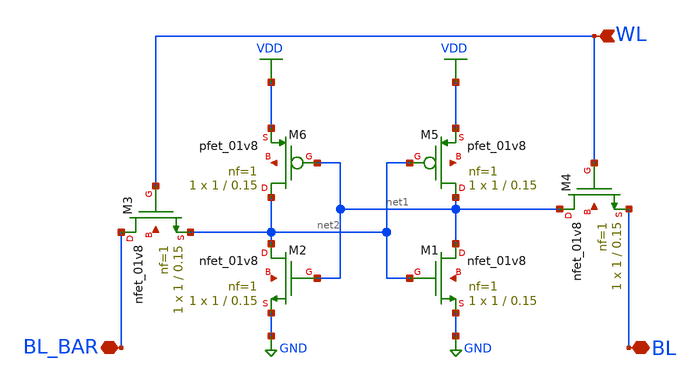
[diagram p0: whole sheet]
** sch_path: analog/schematics/SRAM_access.sch
**.subckt SRAM_access BL_BAR BL WL
*.iopin BL_BAR
*.iopin BL
*.ipin WL
XM1 net1 net2 GND net3 sky130_fd_pr__nfet_01v8 L=0.15 W=1 nf=1 ad='int((nf+1)/2) * W/nf * 0.29' as='int((nf+2)/2) * W/nf * 0.29'
+ pd='2*int((nf+1)/2) * (W/nf + 0.29)' ps='2*int((nf+2)/2) * (W/nf + 0.29)' nrd='0.29 / W' nrs='0.29 / W'
+ sa=0 sb=0 sd=0 mult=1 m=1
XM2 net2 net1 GND net4 sky130_fd_pr__nfet_01v8 L=0.15 W=1 nf=1 ad='int((nf+1)/2) * W/nf * 0.29' as='int((nf+2)/2) * W/nf * 0.29'
+ pd='2*int((nf+1)/2) * (W/nf + 0.29)' ps='2*int((nf+2)/2) * (W/nf + 0.29)' nrd='0.29 / W' nrs='0.29 / W'
+ sa=0 sb=0 sd=0 mult=1 m=1
XM3 BL_BAR WL net2 net5 sky130_fd_pr__nfet_01v8 L=0.15 W=1 nf=1 ad='int((nf+1)/2) * W/nf * 0.29' as='int((nf+2)/2) * W/nf * 0.29'
+ pd='2*int((nf+1)/2) * (W/nf + 0.29)' ps='2*int((nf+2)/2) * (W/nf + 0.29)' nrd='0.29 / W' nrs='0.29 / W'
+ sa=0 sb=0 sd=0 mult=1 m=1
XM4 net1 WL BL net6 sky130_fd_pr__nfet_01v8 L=0.15 W=1 nf=1 ad='int((nf+1)/2) * W/nf * 0.29' as='int((nf+2)/2) * W/nf * 0.29'
+ pd='2*int((nf+1)/2) * (W/nf + 0.29)' ps='2*int((nf+2)/2) * (W/nf + 0.29)' nrd='0.29 / W' nrs='0.29 / W'
+ sa=0 sb=0 sd=0 mult=1 m=1
XM5 net1 net2 VDD net7 sky130_fd_pr__pfet_01v8 L=0.15 W=1 nf=1 ad='int((nf+1)/2) * W/nf * 0.29' as='int((nf+2)/2) * W/nf * 0.29'
+ pd='2*int((nf+1)/2) * (W/nf + 0.29)' ps='2*int((nf+2)/2) * (W/nf + 0.29)' nrd='0.29 / W' nrs='0.29 / W'
+ sa=0 sb=0 sd=0 mult=1 m=1
XM6 net2 net1 VDD net8 sky130_fd_pr__pfet_01v8 L=0.15 W=1 nf=1 ad='int((nf+1)/2) * W/nf * 0.29' as='int((nf+2)/2) * W/nf * 0.29'
+ pd='2*int((nf+1)/2) * (W/nf + 0.29)' ps='2*int((nf+2)/2) * (W/nf + 0.29)' nrd='0.29 / W' nrs='0.29 / W'
+ sa=0 sb=0 sd=0 mult=1 m=1
**.ends
.GLOBAL VDD
.GLOBAL GND
.end
